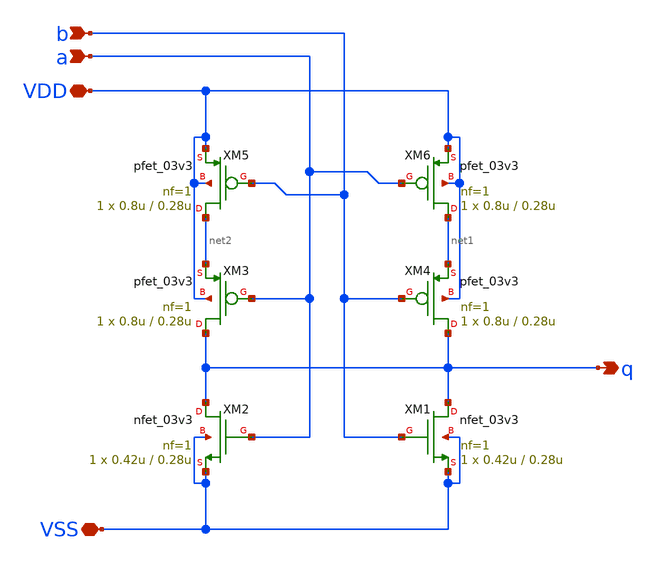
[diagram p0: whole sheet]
** sch_path: adc_sar_nor.sch
**.subckt adc_sar_nor VDD VSS b a q
*.iopin VDD
*.iopin VSS
*.ipin b
*.ipin a
*.opin q
XM1 q b VSS VSS nfet_03v3 L=0.28u W=0.42u nf=1 ad='int((nf+1)/2) * W/nf * 0.18u' as='int((nf+2)/2) * W/nf * 0.18u'
+ pd='2*int((nf+1)/2) * (W/nf + 0.18u)' ps='2*int((nf+2)/2) * (W/nf + 0.18u)' nrd='0.18u / W' nrs='0.18u / W'
+ sa=0 sb=0 sd=0 m=1
XM2 q a VSS VSS nfet_03v3 L=0.28u W=0.42u nf=1 ad='int((nf+1)/2) * W/nf * 0.18u' as='int((nf+2)/2) * W/nf * 0.18u'
+ pd='2*int((nf+1)/2) * (W/nf + 0.18u)' ps='2*int((nf+2)/2) * (W/nf + 0.18u)' nrd='0.18u / W' nrs='0.18u / W'
+ sa=0 sb=0 sd=0 m=1
XM5 net2 b VDD VDD pfet_03v3 L=0.28u W=0.8u nf=1 ad='int((nf+1)/2) * W/nf * 0.18u' as='int((nf+2)/2) * W/nf * 0.18u'
+ pd='2*int((nf+1)/2) * (W/nf + 0.18u)' ps='2*int((nf+2)/2) * (W/nf + 0.18u)' nrd='0.18u / W' nrs='0.18u / W'
+ sa=0 sb=0 sd=0 m=1
XM3 q a net2 VDD pfet_03v3 L=0.28u W=0.8u nf=1 ad='int((nf+1)/2) * W/nf * 0.18u' as='int((nf+2)/2) * W/nf * 0.18u'
+ pd='2*int((nf+1)/2) * (W/nf + 0.18u)' ps='2*int((nf+2)/2) * (W/nf + 0.18u)' nrd='0.18u / W' nrs='0.18u / W'
+ sa=0 sb=0 sd=0 m=1
XM4 q b net1 VDD pfet_03v3 L=0.28u W=0.8u nf=1 ad='int((nf+1)/2) * W/nf * 0.18u' as='int((nf+2)/2) * W/nf * 0.18u'
+ pd='2*int((nf+1)/2) * (W/nf + 0.18u)' ps='2*int((nf+2)/2) * (W/nf + 0.18u)' nrd='0.18u / W' nrs='0.18u / W'
+ sa=0 sb=0 sd=0 m=1
XM6 net1 a VDD VDD pfet_03v3 L=0.28u W=0.8u nf=1 ad='int((nf+1)/2) * W/nf * 0.18u' as='int((nf+2)/2) * W/nf * 0.18u'
+ pd='2*int((nf+1)/2) * (W/nf + 0.18u)' ps='2*int((nf+2)/2) * (W/nf + 0.18u)' nrd='0.18u / W' nrs='0.18u / W'
+ sa=0 sb=0 sd=0 m=1
**.ends
.end
